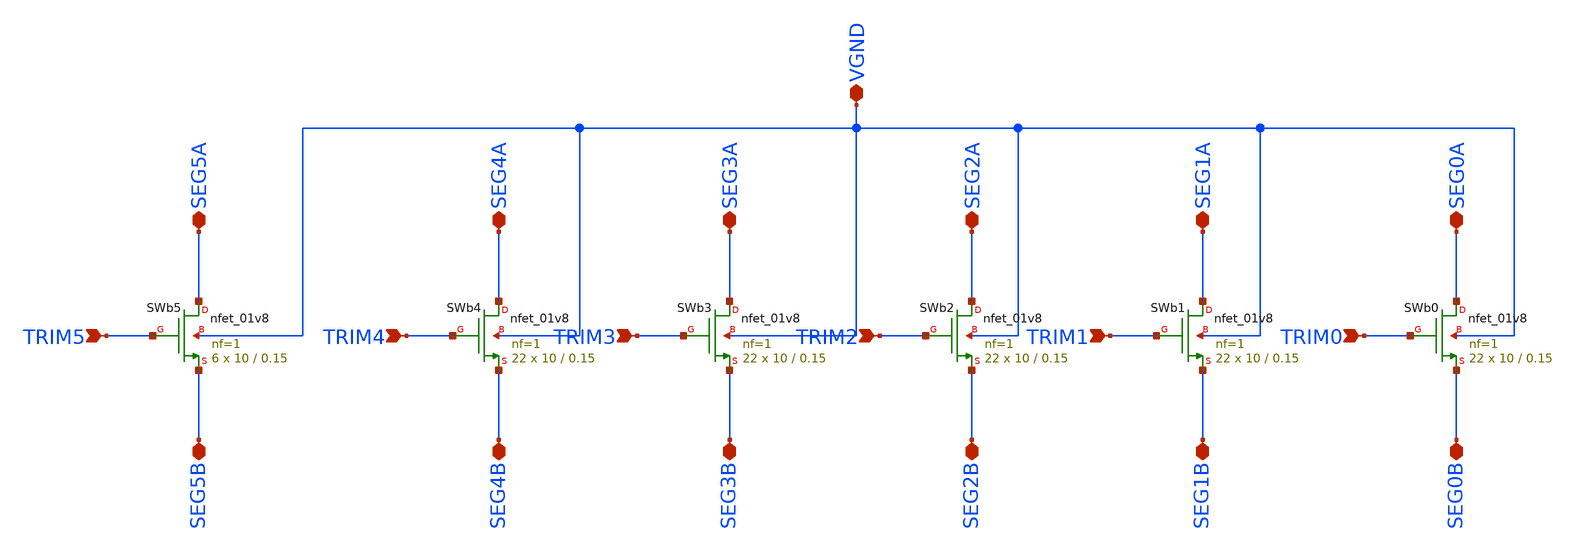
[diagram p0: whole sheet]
** sch_path: designs/bgr_ldo/bgr/trim_sw.sch
**.subckt trim_sw TRIM0 TRIM2 TRIM3 TRIM4 SEG0A SEG0B SEG2A SEG3A SEG4A SEG2B SEG3B SEG4B VGND TRIM1
*+ SEG1A SEG1B TRIM5 SEG5A SEG5B
*.ipin TRIM0
*.ipin TRIM2
*.ipin TRIM3
*.ipin TRIM4
*.iopin SEG0A
*.iopin SEG0B
*.iopin SEG2A
*.iopin SEG3A
*.iopin SEG4A
*.iopin SEG2B
*.iopin SEG3B
*.iopin SEG4B
*.iopin VGND
*.ipin TRIM1
*.iopin SEG1A
*.iopin SEG1B
*.ipin TRIM5
*.iopin SEG5A
*.iopin SEG5B
XSWb0 SEG0A TRIM0 SEG0B VGND sky130_fd_pr__nfet_01v8 L=0.15 W=10 nf=1 ad='int((1 + 1)/2) * 10 / 1 * 0.29'
+ as='int((1 + 2)/2) * 10 / 1 * 0.29' pd='2*int((1 + 1)/2) * (10 / 1 + 0.29)' ps='2*int((1 + 2)/2) * (10 / 1 + 0.29)'
+ nrd='0.29 / 10 ' nrs='0.29 / 10 ' sa=0 sb=0 sd=0 mult=22 m=22
XSWb2 SEG2A TRIM2 SEG2B VGND sky130_fd_pr__nfet_01v8 L=0.15 W=10 nf=1 ad='int((1 + 1)/2) * 10 / 1 * 0.29'
+ as='int((1 + 2)/2) * 10 / 1 * 0.29' pd='2*int((1 + 1)/2) * (10 / 1 + 0.29)' ps='2*int((1 + 2)/2) * (10 / 1 + 0.29)'
+ nrd='0.29 / 10 ' nrs='0.29 / 10 ' sa=0 sb=0 sd=0 mult=22 m=22
XSWb3 SEG3A TRIM3 SEG3B VGND sky130_fd_pr__nfet_01v8 L=0.15 W=10 nf=1 ad='int((1 + 1)/2) * 10 / 1 * 0.29'
+ as='int((1 + 2)/2) * 10 / 1 * 0.29' pd='2*int((1 + 1)/2) * (10 / 1 + 0.29)' ps='2*int((1 + 2)/2) * (10 / 1 + 0.29)'
+ nrd='0.29 / 10 ' nrs='0.29 / 10 ' sa=0 sb=0 sd=0 mult=22 m=22
XSWb4 SEG4A TRIM4 SEG4B VGND sky130_fd_pr__nfet_01v8 L=0.15 W=10 nf=1 ad='int((1 + 1)/2) * 10 / 1 * 0.29'
+ as='int((1 + 2)/2) * 10 / 1 * 0.29' pd='2*int((1 + 1)/2) * (10 / 1 + 0.29)' ps='2*int((1 + 2)/2) * (10 / 1 + 0.29)'
+ nrd='0.29 / 10 ' nrs='0.29 / 10 ' sa=0 sb=0 sd=0 mult=22 m=22
XSWb1 SEG1A TRIM1 SEG1B VGND sky130_fd_pr__nfet_01v8 L=0.15 W=10 nf=1 ad='int((1 + 1)/2) * 10 / 1 * 0.29'
+ as='int((1 + 2)/2) * 10 / 1 * 0.29' pd='2*int((1 + 1)/2) * (10 / 1 + 0.29)' ps='2*int((1 + 2)/2) * (10 / 1 + 0.29)'
+ nrd='0.29 / 10 ' nrs='0.29 / 10 ' sa=0 sb=0 sd=0 mult=22 m=22
XSWb5 SEG5A TRIM5 SEG5B VGND sky130_fd_pr__nfet_01v8 L=0.15 W=10 nf=1 ad='int((1 + 1)/2) * 10 / 1 * 0.29'
+ as='int((1 + 2)/2) * 10 / 1 * 0.29' pd='2*int((1 + 1)/2) * (10 / 1 + 0.29)' ps='2*int((1 + 2)/2) * (10 / 1 + 0.29)'
+ nrd='0.29 / 10 ' nrs='0.29 / 10 ' sa=0 sb=0 sd=0 mult=6 m=6
**.ends
.end
